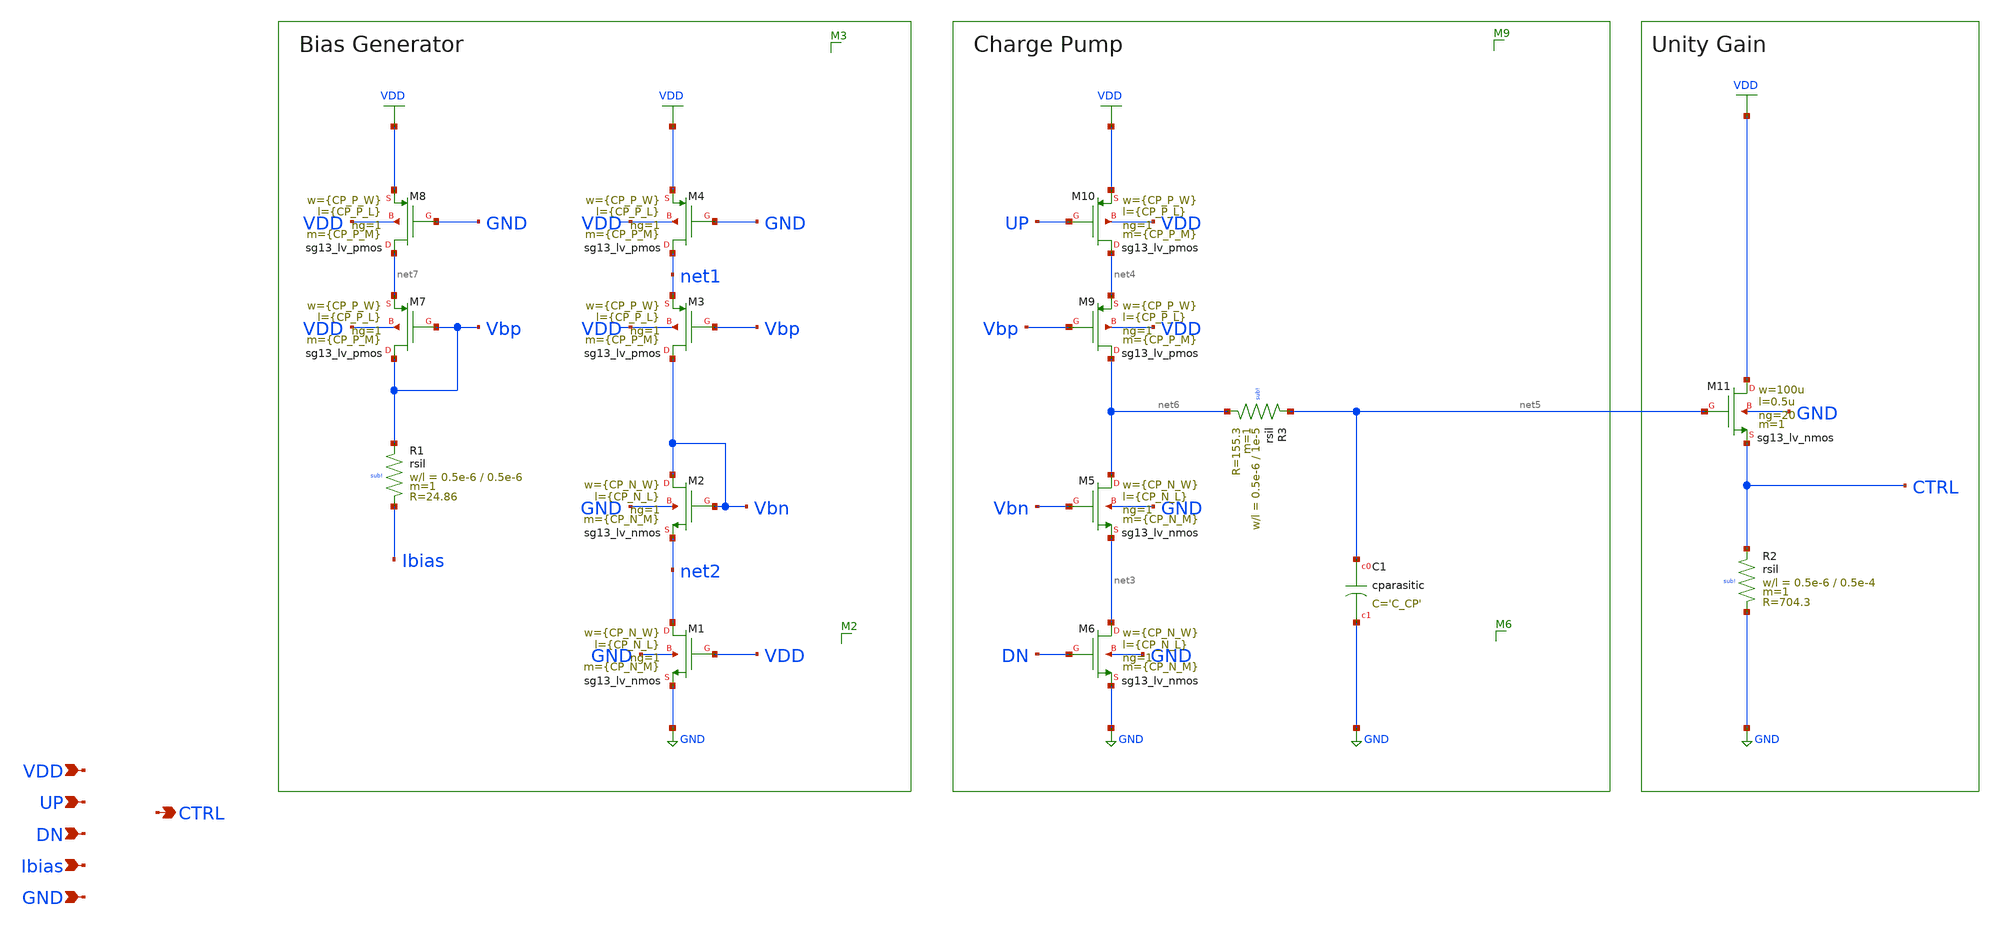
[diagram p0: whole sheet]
** sch_path: schematic/blocks/charge-pump/CP.sch
**.subckt CP CTRL UP VDD Ibias DN GND
*.opin CTRL
*.ipin UP
*.ipin VDD
*.ipin Ibias
*.ipin DN
*.ipin GND
XM2 Vbn Vbn net2 GND sg13_lv_nmos w={CP_N_W} l={CP_N_L} ng=1 m={CP_N_M} mm_ok=1
XM1 net2 VDD GND GND sg13_lv_nmos w={CP_N_W} l={CP_N_L} ng=1 m={CP_N_M} mm_ok=1
XM3 Vbn Vbp net1 VDD sg13_lv_pmos w={CP_P_W} l={CP_P_L} ng=1 m={CP_P_M} mm_ok=1
XM4 net1 GND VDD VDD sg13_lv_pmos w={CP_P_W} l={CP_P_L} ng=1 m={CP_P_M} mm_ok=1
XM7 Vbp Vbp net7 VDD sg13_lv_pmos w={CP_P_W} l={CP_P_L} ng=1 m={CP_P_M} mm_ok=1
XM8 net7 GND VDD VDD sg13_lv_pmos w={CP_P_W} l={CP_P_L} ng=1 m={CP_P_M} mm_ok=1
XM5 net6 Vbn net3 GND sg13_lv_nmos w={CP_N_W} l={CP_N_L} ng=1 m={CP_N_M} mm_ok=1
XM6 net3 DN GND GND sg13_lv_nmos w={CP_N_W} l={CP_N_L} ng=1 m={CP_N_M} mm_ok=1
XM9 net6 Vbp net4 VDD sg13_lv_pmos w={CP_P_W} l={CP_P_L} ng=1 m={CP_P_M} mm_ok=1
XM10 net4 UP VDD VDD sg13_lv_pmos w={CP_P_W} l={CP_P_L} ng=1 m={CP_P_M} mm_ok=1
XC1 net5 GND cparasitic C='C_CP'
XR1 Vbp Ibias sub! rsil w=0.5e-6 l=0.5e-6 m=1 mm_ok=1
XM11 VDD net5 CTRL GND sg13_lv_nmos w=100u l=0.5u ng=20 m=1 mm_ok=1
XR2 CTRL GND sub! rsil w=0.5e-6 l=0.5e-4 m=1 mm_ok=1
XR3 net5 net6 sub! rsil w=0.5e-6 l=1e-5 m=1 mm_ok=1
**.ends
.GLOBAL GND
.GLOBAL VDD
.end
